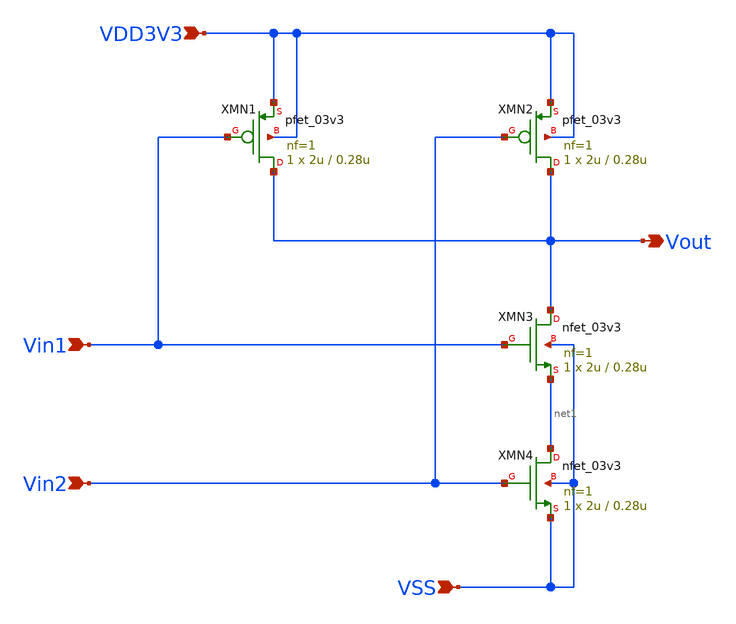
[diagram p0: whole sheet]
** sch_path: designs/libs/core_ina/ina_nand/ina_nand.sch
**.subckt ina_nand VDD3V3 Vin1 Vin2 VSS Vout
*.ipin VDD3V3
*.ipin Vin1
*.ipin Vin2
*.ipin VSS
*.opin Vout
XMN1 Vout Vin1 VDD3V3 VDD3V3 pfet_03v3 L=0.28u W=2u nf=1 ad='int((nf+1)/2) * W/nf * 0.18u' as='int((nf+2)/2) * W/nf * 0.18u'
+ pd='2*int((nf+1)/2) * (W/nf + 0.18u)' ps='2*int((nf+2)/2) * (W/nf + 0.18u)' nrd='0.18u / W' nrs='0.18u / W'
+ sa=0 sb=0 sd=0 m=1
XMN2 Vout Vin2 VDD3V3 VDD3V3 pfet_03v3 L=0.28u W=2u nf=1 ad='int((nf+1)/2) * W/nf * 0.18u' as='int((nf+2)/2) * W/nf * 0.18u'
+ pd='2*int((nf+1)/2) * (W/nf + 0.18u)' ps='2*int((nf+2)/2) * (W/nf + 0.18u)' nrd='0.18u / W' nrs='0.18u / W'
+ sa=0 sb=0 sd=0 m=1
XMN3 Vout Vin1 net1 VSS nfet_03v3 L=0.28u W=2u nf=1 ad='int((nf+1)/2) * W/nf * 0.18u' as='int((nf+2)/2) * W/nf * 0.18u'
+ pd='2*int((nf+1)/2) * (W/nf + 0.18u)' ps='2*int((nf+2)/2) * (W/nf + 0.18u)' nrd='0.18u / W' nrs='0.18u / W'
+ sa=0 sb=0 sd=0 m=1
XMN4 net1 Vin2 VSS VSS nfet_03v3 L=0.28u W=2u nf=1 ad='int((nf+1)/2) * W/nf * 0.18u' as='int((nf+2)/2) * W/nf * 0.18u'
+ pd='2*int((nf+1)/2) * (W/nf + 0.18u)' ps='2*int((nf+2)/2) * (W/nf + 0.18u)' nrd='0.18u / W' nrs='0.18u / W'
+ sa=0 sb=0 sd=0 m=1
**.ends
.end
